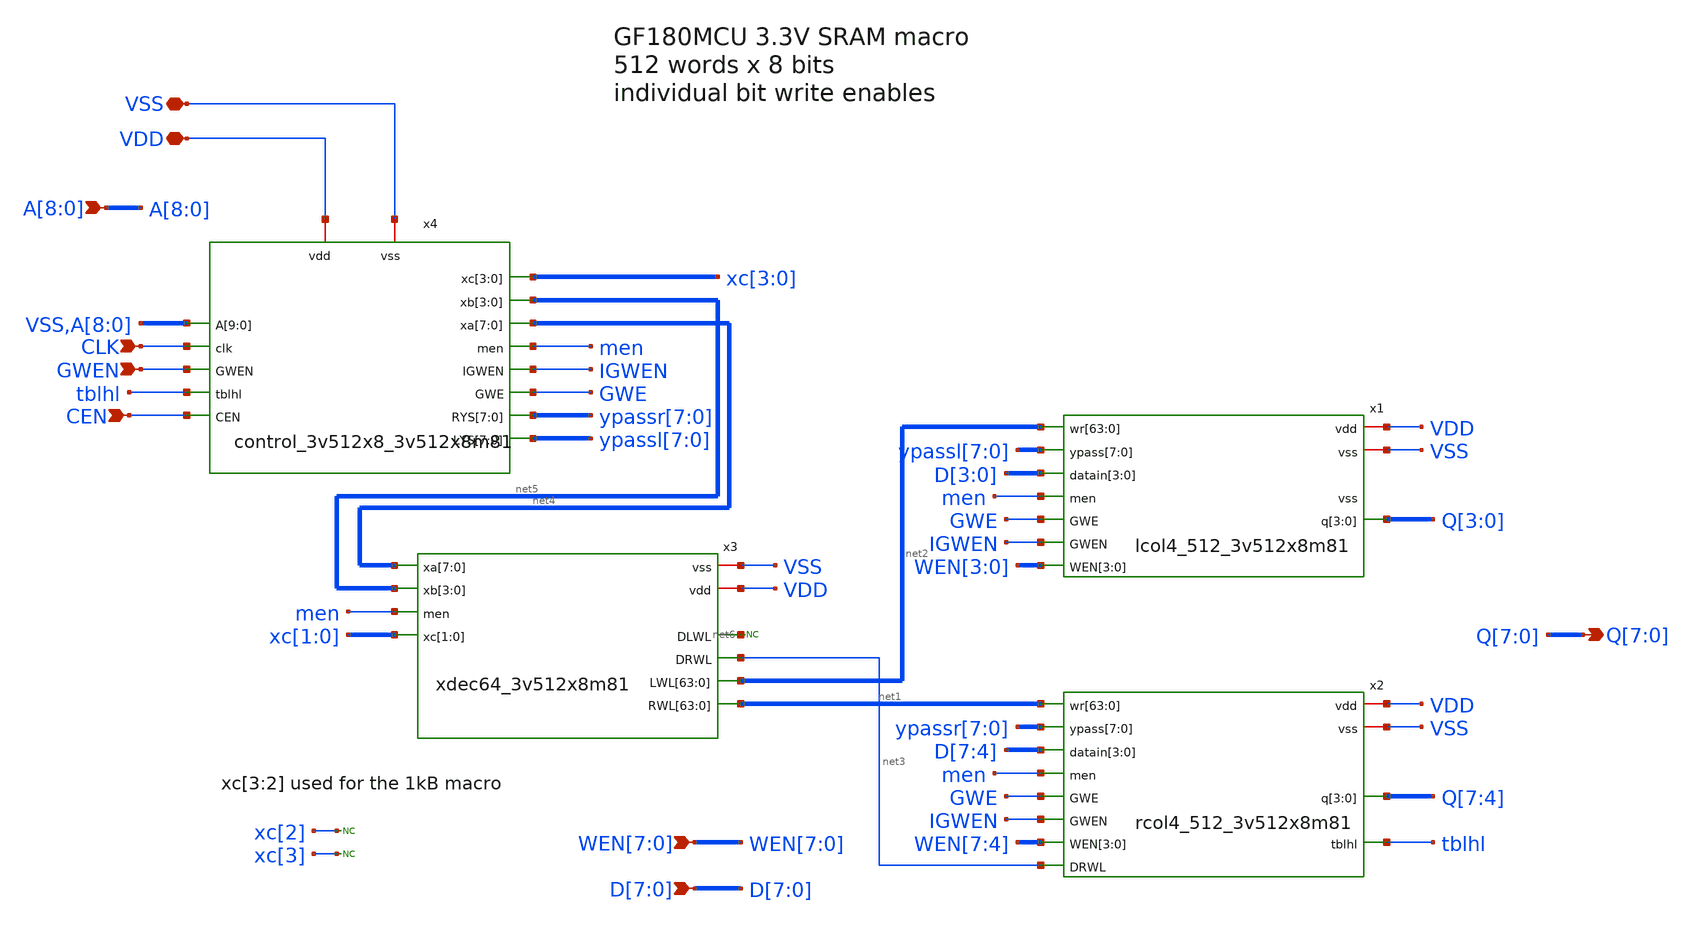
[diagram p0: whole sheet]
** sch_path: cells/gf180mcu_ocd_ip_sram__sram512x8m8wm1/xschem/gf180mcu_ocd_ip_sram__sram512x8m8wm1.sch
**.subckt gf180mcu_ocd_ip_sram__sram512x8m8wm1 Q[7],Q[6],Q[5],Q[4],Q[3],Q[2],Q[1],Q[0]
*+ WEN[7],WEN[6],WEN[5],WEN[4],WEN[3],WEN[2],WEN[1],WEN[0] D[7],D[6],D[5],D[4],D[3],D[2],D[1],D[0] A[8],A[7],A[6],A[5],A[4],A[3],A[2],A[1],A[0] CLK GWEN VDD
*+ VSS CEN
*.opin Q[7],Q[6],Q[5],Q[4],Q[3],Q[2],Q[1],Q[0]
*.ipin WEN[7],WEN[6],WEN[5],WEN[4],WEN[3],WEN[2],WEN[1],WEN[0]
*.ipin D[7],D[6],D[5],D[4],D[3],D[2],D[1],D[0]
*.ipin A[8],A[7],A[6],A[5],A[4],A[3],A[2],A[1],A[0]
*.ipin CLK
*.ipin GWEN
*.iopin VDD
*.iopin VSS
*.ipin CEN
x1 VDD VSS net2[63] net2[62] net2[61] net2[60] net2[59] net2[58] net2[57] net2[56] net2[55] net2[54]
+ net2[53] net2[52] net2[51] net2[50] net2[49] net2[48] net2[47] net2[46] net2[45] net2[44] net2[43] net2[42]
+ net2[41] net2[40] net2[39] net2[38] net2[37] net2[36] net2[35] net2[34] net2[33] net2[32] net2[31] net2[30]
+ net2[29] net2[28] net2[27] net2[26] net2[25] net2[24] net2[23] net2[22] net2[21] net2[20] net2[19] net2[18]
+ net2[17] net2[16] net2[15] net2[14] net2[13] net2[12] net2[11] net2[10] net2[9] net2[8] net2[7] net2[6]
+ net2[5] net2[4] net2[3] net2[2] net2[1] net2[0] ypassl[7] ypassl[6] ypassl[5] ypassl[4] ypassl[3] ypassl[2]
+ ypassl[1] ypassl[0] D[3] D[2] D[1] D[0] Q[3] Q[2] Q[1] Q[0] men GWE IGWEN WEN[3] WEN[2] WEN[1] WEN[0]
+ lcol4_512_3v512x8m81
x2 VDD VSS net1[63] net1[62] net1[61] net1[60] net1[59] net1[58] net1[57] net1[56] net1[55] net1[54]
+ net1[53] net1[52] net1[51] net1[50] net1[49] net1[48] net1[47] net1[46] net1[45] net1[44] net1[43] net1[42]
+ net1[41] net1[40] net1[39] net1[38] net1[37] net1[36] net1[35] net1[34] net1[33] net1[32] net1[31] net1[30]
+ net1[29] net1[28] net1[27] net1[26] net1[25] net1[24] net1[23] net1[22] net1[21] net1[20] net1[19] net1[18]
+ net1[17] net1[16] net1[15] net1[14] net1[13] net1[12] net1[11] net1[10] net1[9] net1[8] net1[7] net1[6]
+ net1[5] net1[4] net1[3] net1[2] net1[1] net1[0] ypassr[7] ypassr[6] ypassr[5] ypassr[4] ypassr[3] ypassr[2]
+ ypassr[1] ypassr[0] D[7] D[6] D[5] D[4] Q[7] Q[6] Q[5] Q[4] men GWE IGWEN WEN[7] WEN[6] WEN[5] WEN[4] net3
+ tblhl rcol4_512_3v512x8m81
x3 VSS VDD net6 net3 net4[7] net4[6] net4[5] net4[4] net4[3] net4[2] net4[1] net4[0] net2[63]
+ net2[62] net2[61] net2[60] net2[59] net2[58] net2[57] net2[56] net2[55] net2[54] net2[53] net2[52] net2[51]
+ net2[50] net2[49] net2[48] net2[47] net2[46] net2[45] net2[44] net2[43] net2[42] net2[41] net2[40] net2[39]
+ net2[38] net2[37] net2[36] net2[35] net2[34] net2[33] net2[32] net2[31] net2[30] net2[29] net2[28] net2[27]
+ net2[26] net2[25] net2[24] net2[23] net2[22] net2[21] net2[20] net2[19] net2[18] net2[17] net2[16] net2[15]
+ net2[14] net2[13] net2[12] net2[11] net2[10] net2[9] net2[8] net2[7] net2[6] net2[5] net2[4] net2[3] net2[2]
+ net2[1] net2[0] net5[3] net5[2] net5[1] net5[0] net1[63] net1[62] net1[61] net1[60] net1[59] net1[58]
+ net1[57] net1[56] net1[55] net1[54] net1[53] net1[52] net1[51] net1[50] net1[49] net1[48] net1[47] net1[46]
+ net1[45] net1[44] net1[43] net1[42] net1[41] net1[40] net1[39] net1[38] net1[37] net1[36] net1[35] net1[34]
+ net1[33] net1[32] net1[31] net1[30] net1[29] net1[28] net1[27] net1[26] net1[25] net1[24] net1[23] net1[22]
+ net1[21] net1[20] net1[19] net1[18] net1[17] net1[16] net1[15] net1[14] net1[13] net1[12] net1[11] net1[10]
+ net1[9] net1[8] net1[7] net1[6] net1[5] net1[4] net1[3] net1[2] net1[1] net1[0] men xc[1] xc[0]
+ xdec64_3v512x8m81
* noconn #net6
x4 VSS VDD VSS A[8] A[7] A[6] A[5] A[4] A[3] A[2] A[1] A[0] xc[3] xc[2] xc[1] xc[0] net5[3] net5[2]
+ net5[1] net5[0] net4[7] net4[6] net4[5] net4[4] net4[3] net4[2] net4[1] net4[0] CLK men IGWEN GWEN GWE
+ ypassr[7] ypassr[6] ypassr[5] ypassr[4] ypassr[3] ypassr[2] ypassr[1] ypassr[0] ypassl[7] ypassl[6] ypassl[5]
+ ypassl[4] ypassl[3] ypassl[2] ypassl[1] ypassl[0] tblhl CEN control_3v512x8_3v512x8m81
* noconn xc[2]
* noconn xc[3]
**.ends
.end
